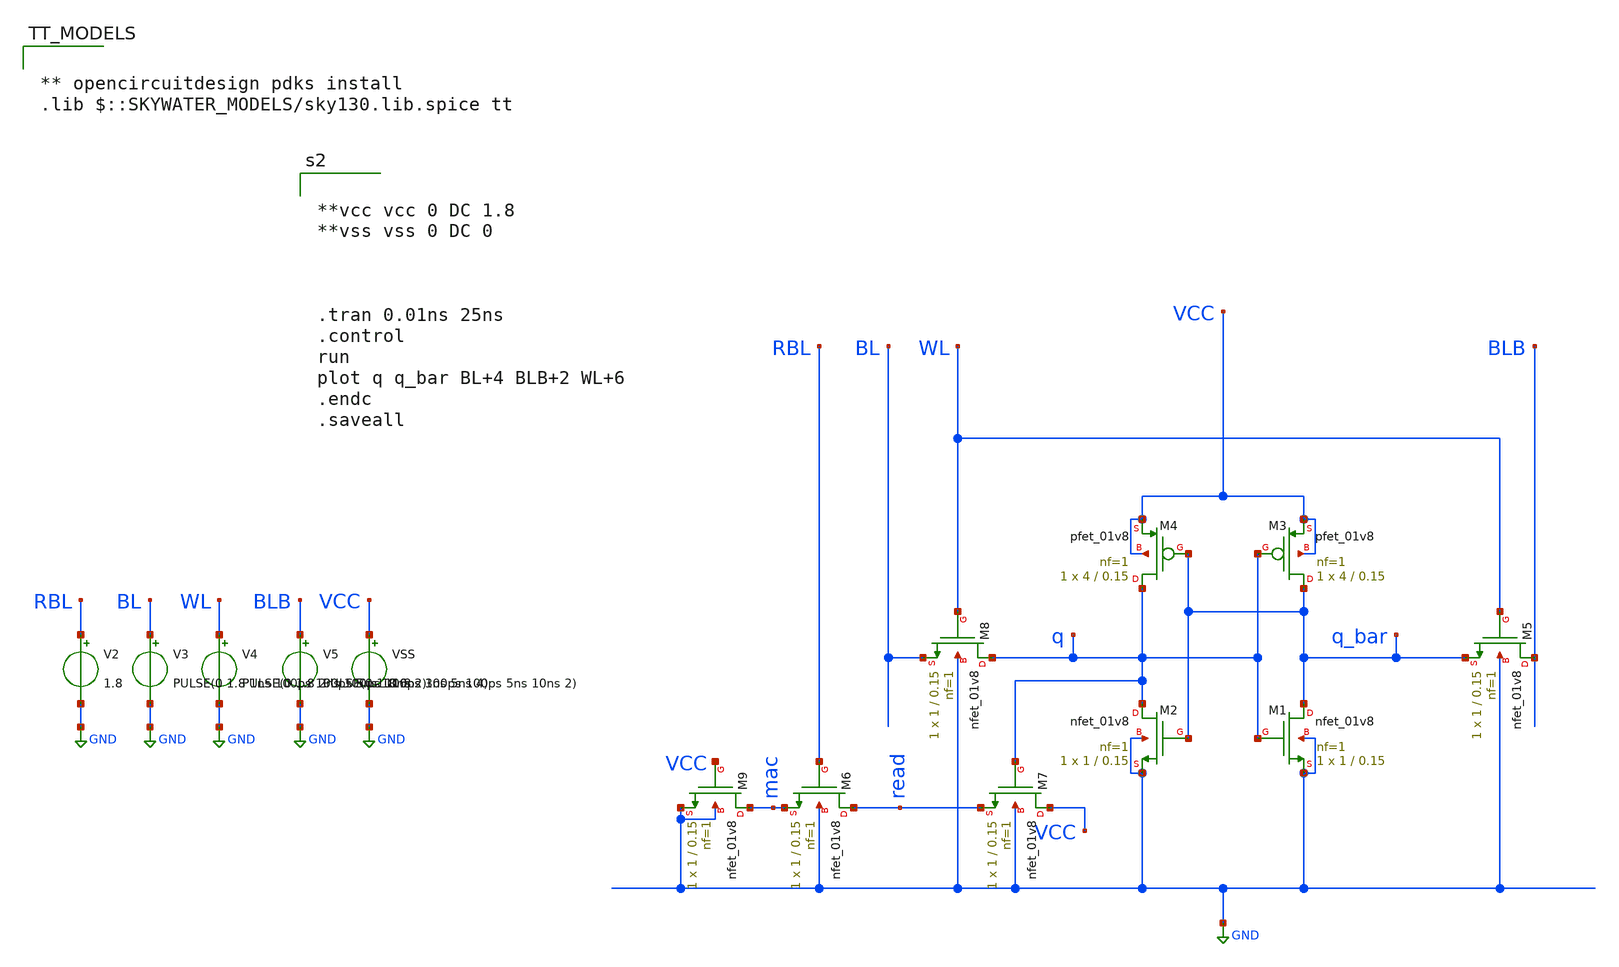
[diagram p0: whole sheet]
** sch_path: 8Tsram_work.sch
**.subckt 8Tsram_work
XM1 q_bar q GND GND sky130_fd_pr__nfet_01v8 L=0.15 W=1 nf=1 ad='int((1 + 1)/2) * 1 / 1 * 0.29' as='int((1 + 2)/2) * 1 / 1 * 0.29'
+ pd='2*int((1 + 1)/2) * (1 / 1 + 0.29)' ps='2*int((1 + 2)/2) * (1 / 1 + 0.29)' nrd='0.29 / 1 ' nrs='0.29 / 1 '
+ sa=0 sb=0 sd=0 mult=1 m=1
XM2 q q_bar GND GND sky130_fd_pr__nfet_01v8 L=0.15 W=1 nf=1 ad='int((1 + 1)/2) * 1 / 1 * 0.29' as='int((1 + 2)/2) * 1 / 1 * 0.29'
+ pd='2*int((1 + 1)/2) * (1 / 1 + 0.29)' ps='2*int((1 + 2)/2) * (1 / 1 + 0.29)' nrd='0.29 / 1 ' nrs='0.29 / 1 '
+ sa=0 sb=0 sd=0 mult=1 m=1
XM3 q_bar q VCC VCC sky130_fd_pr__pfet_01v8 L=0.15 W=4 nf=1 ad='int((1 + 1)/2) * 4 / 1 * 0.29' as='int((1 + 2)/2) * 4 / 1 * 0.29'
+ pd='2*int((1 + 1)/2) * (4 / 1 + 0.29)' ps='2*int((1 + 2)/2) * (4 / 1 + 0.29)' nrd='0.29 / 4 ' nrs='0.29 / 4 '
+ sa=0 sb=0 sd=0 mult=1 m=1
XM4 q q_bar VCC VCC sky130_fd_pr__pfet_01v8 L=0.15 W=4 nf=1 ad='int((1 + 1)/2) * 4 / 1 * 0.29' as='int((1 + 2)/2) * 4 / 1 * 0.29'
+ pd='2*int((1 + 1)/2) * (4 / 1 + 0.29)' ps='2*int((1 + 2)/2) * (4 / 1 + 0.29)' nrd='0.29 / 4 ' nrs='0.29 / 4 '
+ sa=0 sb=0 sd=0 mult=1 m=1
XM5 BLB WL q_bar GND sky130_fd_pr__nfet_01v8 L=0.15 W=1 nf=1 ad='int((1 + 1)/2) * 1 / 1 * 0.29' as='int((1 + 2)/2) * 1 / 1 * 0.29'
+ pd='2*int((1 + 1)/2) * (1 / 1 + 0.29)' ps='2*int((1 + 2)/2) * (1 / 1 + 0.29)' nrd='0.29 / 1 ' nrs='0.29 / 1 '
+ sa=0 sb=0 sd=0 mult=1 m=1
XM8 q WL BL GND sky130_fd_pr__nfet_01v8 L=0.15 W=1 nf=1 ad='int((1 + 1)/2) * 1 / 1 * 0.29' as='int((1 + 2)/2) * 1 / 1 * 0.29'
+ pd='2*int((1 + 1)/2) * (1 / 1 + 0.29)' ps='2*int((1 + 2)/2) * (1 / 1 + 0.29)' nrd='0.29 / 1 ' nrs='0.29 / 1 '
+ sa=0 sb=0 sd=0 mult=1 m=1
V2 RBL GND 1.8
V3 BL GND PULSE(0 1.8 1ns 100ps 100ps 5ns 10ns 2)
V4 WL GND PULSE(0 1.8 2ns 100ps 100ps 3ns 5ns 4)
V5 BLB GND PULSE(0 1.8 6ns 100ps 100ps 5ns 10ns 2)
XM9 mac VCC GND GND sky130_fd_pr__nfet_01v8 L=0.15 W=1 nf=1 ad='int((1 + 1)/2) * 1 / 1 * 0.29' as='int((1 + 2)/2) * 1 / 1 * 0.29'
+ pd='2*int((1 + 1)/2) * (1 / 1 + 0.29)' ps='2*int((1 + 2)/2) * (1 / 1 + 0.29)' nrd='0.29 / 1 ' nrs='0.29 / 1 '
+ sa=0 sb=0 sd=0 mult=1 m=1
VSS VCC GND 1.8
XM6 read RBL mac GND sky130_fd_pr__nfet_01v8 L=0.15 W=1 nf=1 ad='int((1 + 1)/2) * 1 / 1 * 0.29' as='int((1 + 2)/2) * 1 / 1 * 0.29'
+ pd='2*int((1 + 1)/2) * (1 / 1 + 0.29)' ps='2*int((1 + 2)/2) * (1 / 1 + 0.29)' nrd='0.29 / 1 ' nrs='0.29 / 1 '
+ sa=0 sb=0 sd=0 mult=1 m=1
XM7 VCC q read GND sky130_fd_pr__nfet_01v8 L=0.15 W=1 nf=1 ad='int((1 + 1)/2) * 1 / 1 * 0.29' as='int((1 + 2)/2) * 1 / 1 * 0.29'
+ pd='2*int((1 + 1)/2) * (1 / 1 + 0.29)' ps='2*int((1 + 2)/2) * (1 / 1 + 0.29)' nrd='0.29 / 1 ' nrs='0.29 / 1 '
+ sa=0 sb=0 sd=0 mult=1 m=1
**** begin user architecture code


**vcc vcc 0 DC 1.8
**vss vss 0 DC 0



.tran 0.01ns 25ns
.control
run
plot q q_bar BL+4 BLB+2 WL+6
.endc
.saveall




** opencircuitdesign pdks install
.lib $::SKYWATER_MODELS/sky130.lib.spice tt

**** end user architecture code
**.ends
.GLOBAL GND
.end
